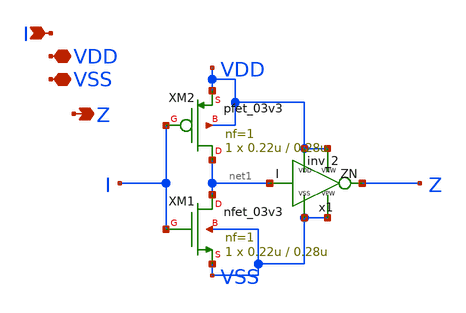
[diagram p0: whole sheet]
** sch_path: xschem/test.sch
**.subckt test I VDD Z VSS
*.ipin I
*.iopin VDD
*.opin Z
*.iopin VSS
XM1 net1 I VSS VSS nfet_03v3 L=0.28u W=0.22u nf=1 ad='int((nf+1)/2) * W/nf * 0.18u' as='int((nf+2)/2) * W/nf * 0.18u'
+ pd='2*int((nf+1)/2) * (W/nf + 0.18u)' ps='2*int((nf+2)/2) * (W/nf + 0.18u)' nrd='0.18u / W' nrs='0.18u / W'
+ sa=0 sb=0 sd=0 m=1
XM2 net1 I VDD VDD pfet_03v3 L=0.28u W=0.22u nf=1 ad='int((nf+1)/2) * W/nf * 0.18u' as='int((nf+2)/2) * W/nf * 0.18u'
+ pd='2*int((nf+1)/2) * (W/nf + 0.18u)' ps='2*int((nf+2)/2) * (W/nf + 0.18u)' nrd='0.18u / W' nrs='0.18u / W'
+ sa=0 sb=0 sd=0 m=1
x1 net1 Z VDD VDD VSS VSS gf180mcu_fd_sc_mcu7t5v0__inv_2
**.ends
.end
